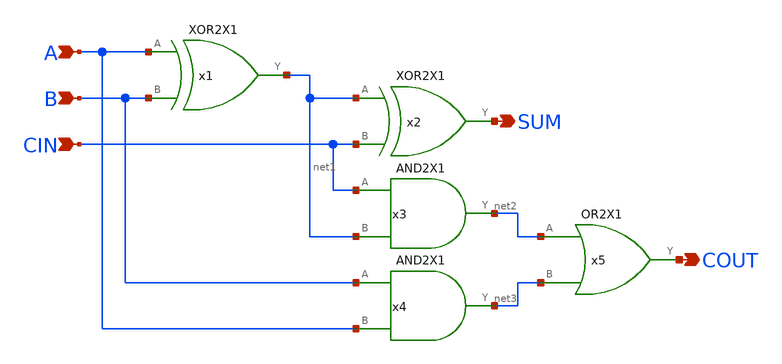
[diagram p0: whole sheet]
** sch_path: lib/xschem/FA.sch
**.subckt FA SUM COUT A B CIN
*.opin SUM
*.opin COUT
*.ipin A
*.ipin B
*.ipin CIN
x1 net1 A B VDD VSS XOR2X1
x2 SUM net1 CIN VDD VSS XOR2X1
x3 net2 CIN net1 VDD VSS AND2X1
x4 net3 B A VDD VSS AND2X1
x5 COUT net2 net3 VDD VSS OR2X1
**.ends
.end
